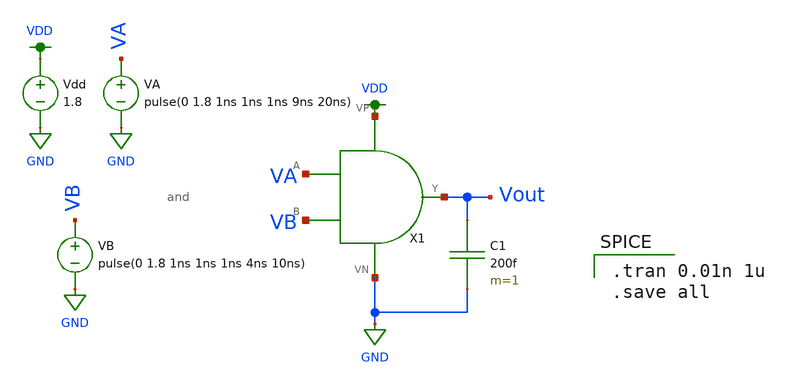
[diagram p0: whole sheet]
** sch_path: mini_proj_1/schematic/and_tran.sch
**.subckt and_tran
X1 Vout VA VB VDD GND and
Vdd VDD GND 1.8
VA VA GND pulse(0 1.8 1ns 1ns 1ns 9ns 20ns)
VB VB GND pulse(0 1.8 1ns 1ns 1ns 4ns 10ns)
C1 Vout GND 200f m=1
**** begin user architecture code

.tran 0.01n 1u
.save all


.option wnflag=1
.lib ~/skywater/skywater-pdk/libraries/sky130_fd_pr_ngspice/latest/models/sky130.lib.spice tt

**** end user architecture code
**.ends

* expanding   symbol:  /home/madvlsi/Documents/madvlsi/mini_proj_1/schematic/and.sym # of pins=5
** sym_path: mini_proj_1/schematic/and.sym
** sch_path: mini_proj_1/schematic/and.sch
.subckt and Y A B VP VN
*.ipin A
*.ipin B
*.iopin VP
*.iopin VN
*.opin Y
X1 net1 A B VP VN nand
X2 VP VN net1 Y inverter
.ends


* expanding   symbol:  /home/madvlsi/Documents/madvlsi/mini_proj_1/schematic/nand.sym # of pins=5
** sym_path: mini_proj_1/schematic/nand.sym
** sch_path: mini_proj_1/schematic/nand.sch
.subckt nand Y A B VP VN
*.ipin A
*.ipin B
*.iopin VP
*.iopin VN
*.opin Y
XM1 Y A VP VP sky130_fd_pr__pfet_01v8 L=0.15 W=1 nf=1 ad='int((nf+1)/2) * W/nf * 0.29' as='int((nf+2)/2) * W/nf * 0.29'
+ pd='2*int((nf+1)/2) * (W/nf + 0.29)' ps='2*int((nf+2)/2) * (W/nf + 0.29)' nrd='0.29 / W' nrs='0.29 / W'
+ sa=0 sb=0 sd=0 mult=1 m=1
XM2 VP B Y VP sky130_fd_pr__pfet_01v8 L=0.15 W=1 nf=1 ad='int((nf+1)/2) * W/nf * 0.29' as='int((nf+2)/2) * W/nf * 0.29'
+ pd='2*int((nf+1)/2) * (W/nf + 0.29)' ps='2*int((nf+2)/2) * (W/nf + 0.29)' nrd='0.29 / W' nrs='0.29 / W'
+ sa=0 sb=0 sd=0 mult=1 m=1
XM3 Y A net1 VN sky130_fd_pr__nfet_01v8 L=0.15 W=1 nf=1 ad='int((nf+1)/2) * W/nf * 0.29' as='int((nf+2)/2) * W/nf * 0.29'
+ pd='2*int((nf+1)/2) * (W/nf + 0.29)' ps='2*int((nf+2)/2) * (W/nf + 0.29)' nrd='0.29 / W' nrs='0.29 / W'
+ sa=0 sb=0 sd=0 mult=1 m=1
XM4 VN B net1 VN sky130_fd_pr__nfet_01v8 L=0.15 W=1 nf=1 ad='int((nf+1)/2) * W/nf * 0.29' as='int((nf+2)/2) * W/nf * 0.29'
+ pd='2*int((nf+1)/2) * (W/nf + 0.29)' ps='2*int((nf+2)/2) * (W/nf + 0.29)' nrd='0.29 / W' nrs='0.29 / W'
+ sa=0 sb=0 sd=0 mult=1 m=1
.ends


* expanding   symbol:  /home/madvlsi/Documents/madvlsi/mini_proj_1/schematic/inverter.sym # of
*+ pins=4
** sym_path: mini_proj_1/schematic/inverter.sym
** sch_path: mini_proj_1/schematic/inverter.sch
.subckt inverter VP VN Vin Vout
*.ipin Vin
*.iopin VP
*.iopin VN
*.opin Vout
XM1 Vout Vin VN VN sky130_fd_pr__nfet_01v8 L=0.15 W=1 nf=1 ad='int((nf+1)/2) * W/nf * 0.29' as='int((nf+2)/2) * W/nf * 0.29'
+ pd='2*int((nf+1)/2) * (W/nf + 0.29)' ps='2*int((nf+2)/2) * (W/nf + 0.29)' nrd='0.29 / W' nrs='0.29 / W'
+ sa=0 sb=0 sd=0 mult=1 m=1
XM2 Vout Vin VP VP sky130_fd_pr__pfet_01v8 L=0.15 W=1 nf=1 ad='int((nf+1)/2) * W/nf * 0.29' as='int((nf+2)/2) * W/nf * 0.29'
+ pd='2*int((nf+1)/2) * (W/nf + 0.29)' ps='2*int((nf+2)/2) * (W/nf + 0.29)' nrd='0.29 / W' nrs='0.29 / W'
+ sa=0 sb=0 sd=0 mult=1 m=1
.ends

.GLOBAL VDD
.GLOBAL GND
.end
